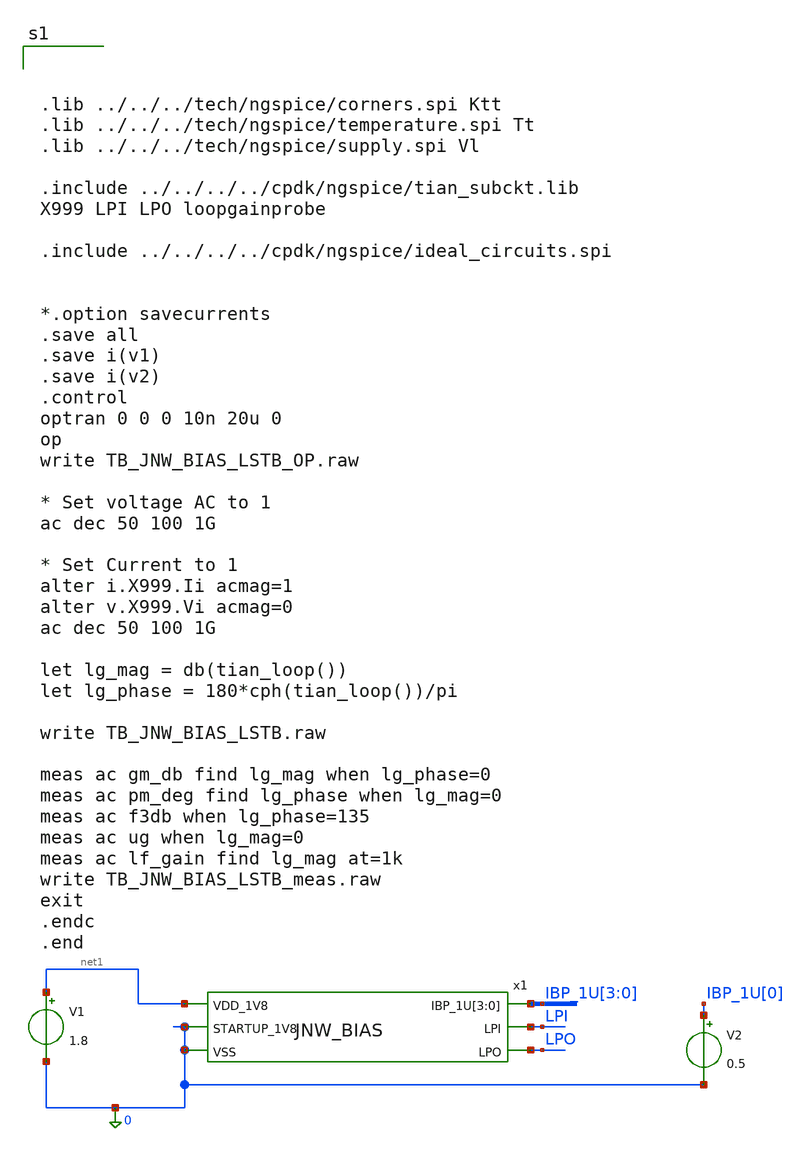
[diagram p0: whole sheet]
** sch_path: design/JNW_BIAS_SKY130A/TB_JNW_BIAS_LSTB.sch
**.subckt TB_JNW_BIAS_LSTB
x1 net1 LPI IBP_1U[3] IBP_1U[2] IBP_1U[1] IBP_1U[0] LPO 0 0 JNW_BIAS
V1 net1 0 1.8
V2 IBP_1U[0] 0 0.5
**** begin user architecture code



.lib ../../../tech/ngspice/corners.spi Ktt
.lib ../../../tech/ngspice/temperature.spi Tt
.lib ../../../tech/ngspice/supply.spi Vl

.include ../../../../cpdk/ngspice/tian_subckt.lib
X999 LPI LPO loopgainprobe

.include ../../../../cpdk/ngspice/ideal_circuits.spi


*.option savecurrents
.save all
.save i(v1)
.save i(v2)
.control
optran 0 0 0 10n 20u 0
op
write TB_JNW_BIAS_LSTB_OP.raw

* Set voltage AC to 1
ac dec 50 100 1G

* Set Current to 1
alter i.X999.Ii acmag=1
alter v.X999.Vi acmag=0
ac dec 50 100 1G

let lg_mag = db(tian_loop())
let lg_phase = 180*cph(tian_loop())/pi

write TB_JNW_BIAS_LSTB.raw

meas ac gm_db find lg_mag when lg_phase=0
meas ac pm_deg find lg_phase when lg_mag=0
meas ac f3db when lg_phase=135
meas ac ug when lg_mag=0
meas ac lf_gain find lg_mag at=1k
write TB_JNW_BIAS_LSTB_meas.raw
exit
.endc
.end



**** end user architecture code
**.ends
.end
